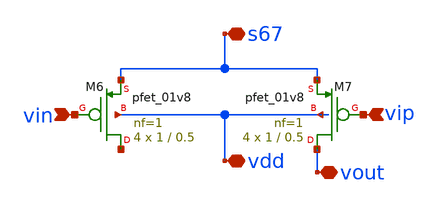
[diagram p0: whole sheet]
** sch_path: opamp/mag/untitled-1.sch
**.subckt untitled-1 vin vip vdd vout s67
*.ipin vin
*.ipin vip
*.iopin vdd
*.iopin vout
*.iopin s67
XM6 net1 vin s67 vdd sky130_fd_pr__pfet_01v8 L=0.5 W=1 nf=1 ad='int((nf+1)/2) * W/nf * 0.29' as='int((nf+2)/2) * W/nf * 0.29'
+ pd='2*int((nf+1)/2) * (W/nf + 0.29)' ps='2*int((nf+2)/2) * (W/nf + 0.29)' nrd='0.29 / W' nrs='0.29 / W'
+ sa=0 sb=0 sd=0 mult=4 m=4
XM7 vout vip s67 vdd sky130_fd_pr__pfet_01v8 L=0.5 W=1 nf=1 ad='int((nf+1)/2) * W/nf * 0.29' as='int((nf+2)/2) * W/nf * 0.29'
+ pd='2*int((nf+1)/2) * (W/nf + 0.29)' ps='2*int((nf+2)/2) * (W/nf + 0.29)' nrd='0.29 / W' nrs='0.29 / W'
+ sa=0 sb=0 sd=0 mult=4 m=4
**.ends
.end
